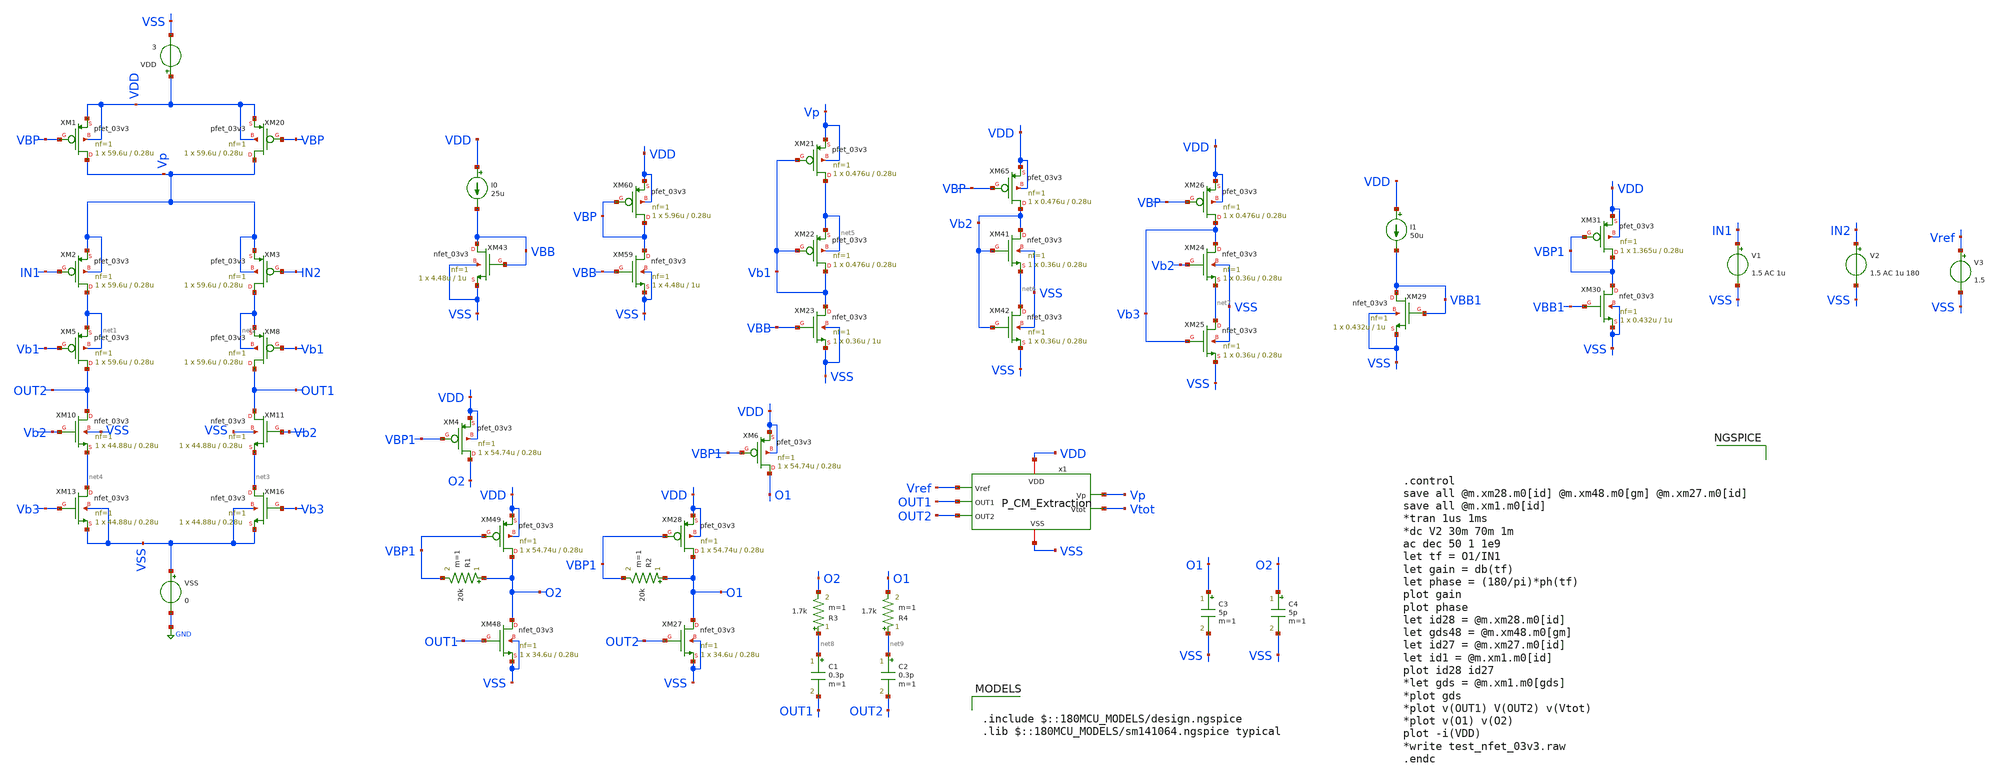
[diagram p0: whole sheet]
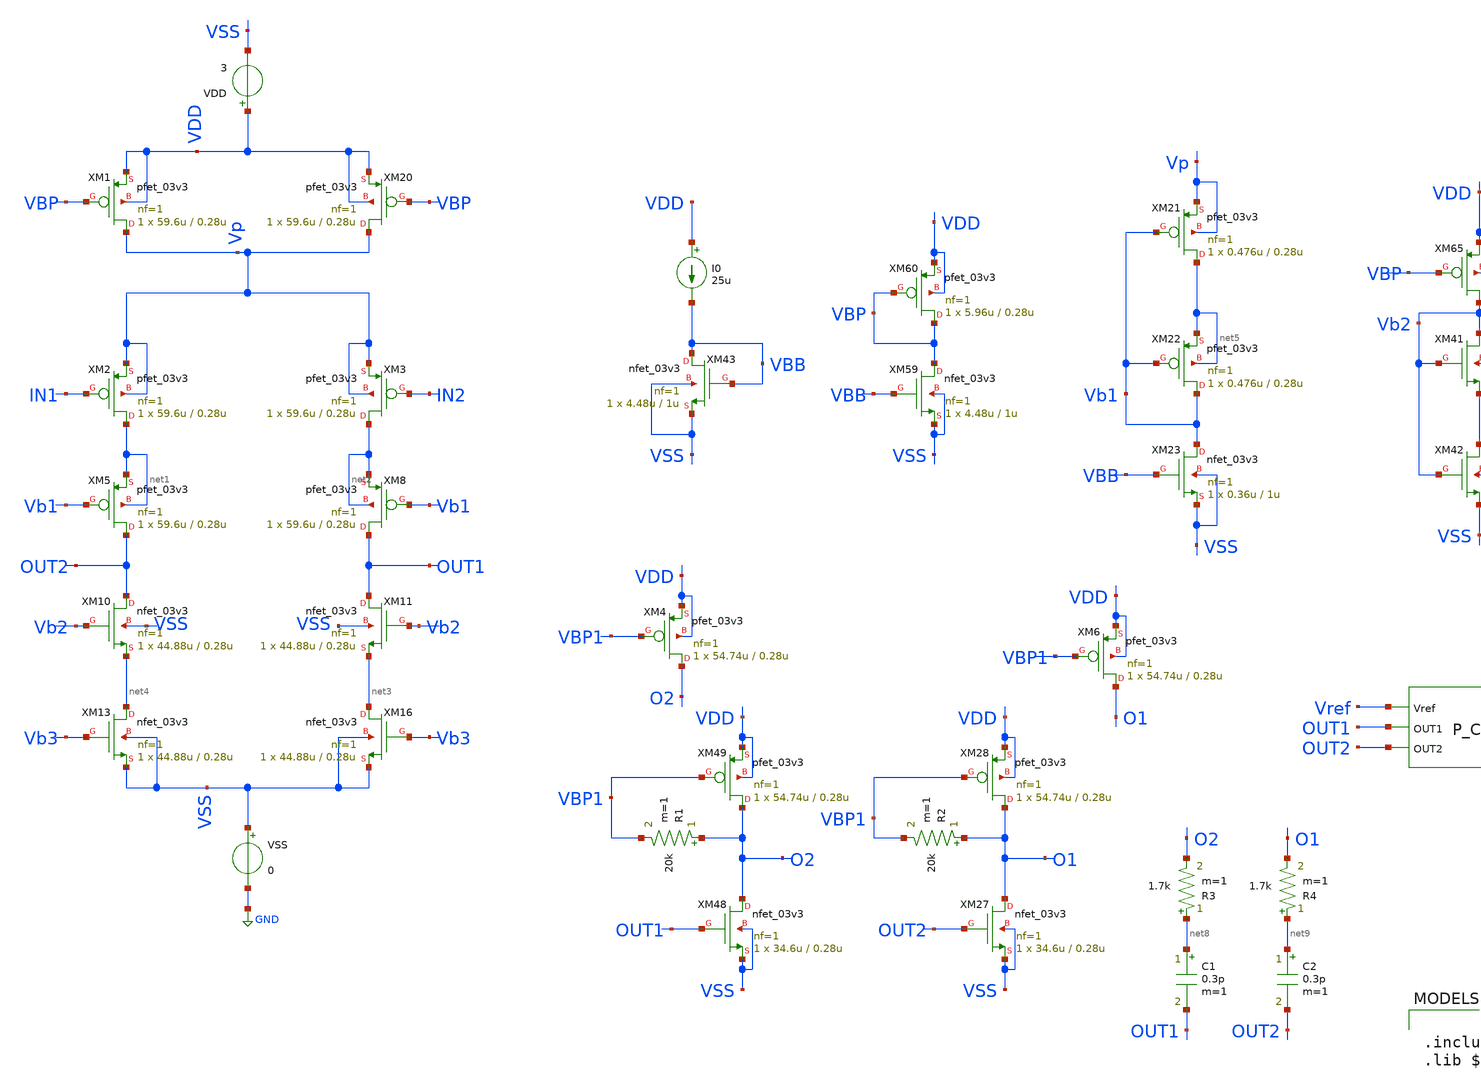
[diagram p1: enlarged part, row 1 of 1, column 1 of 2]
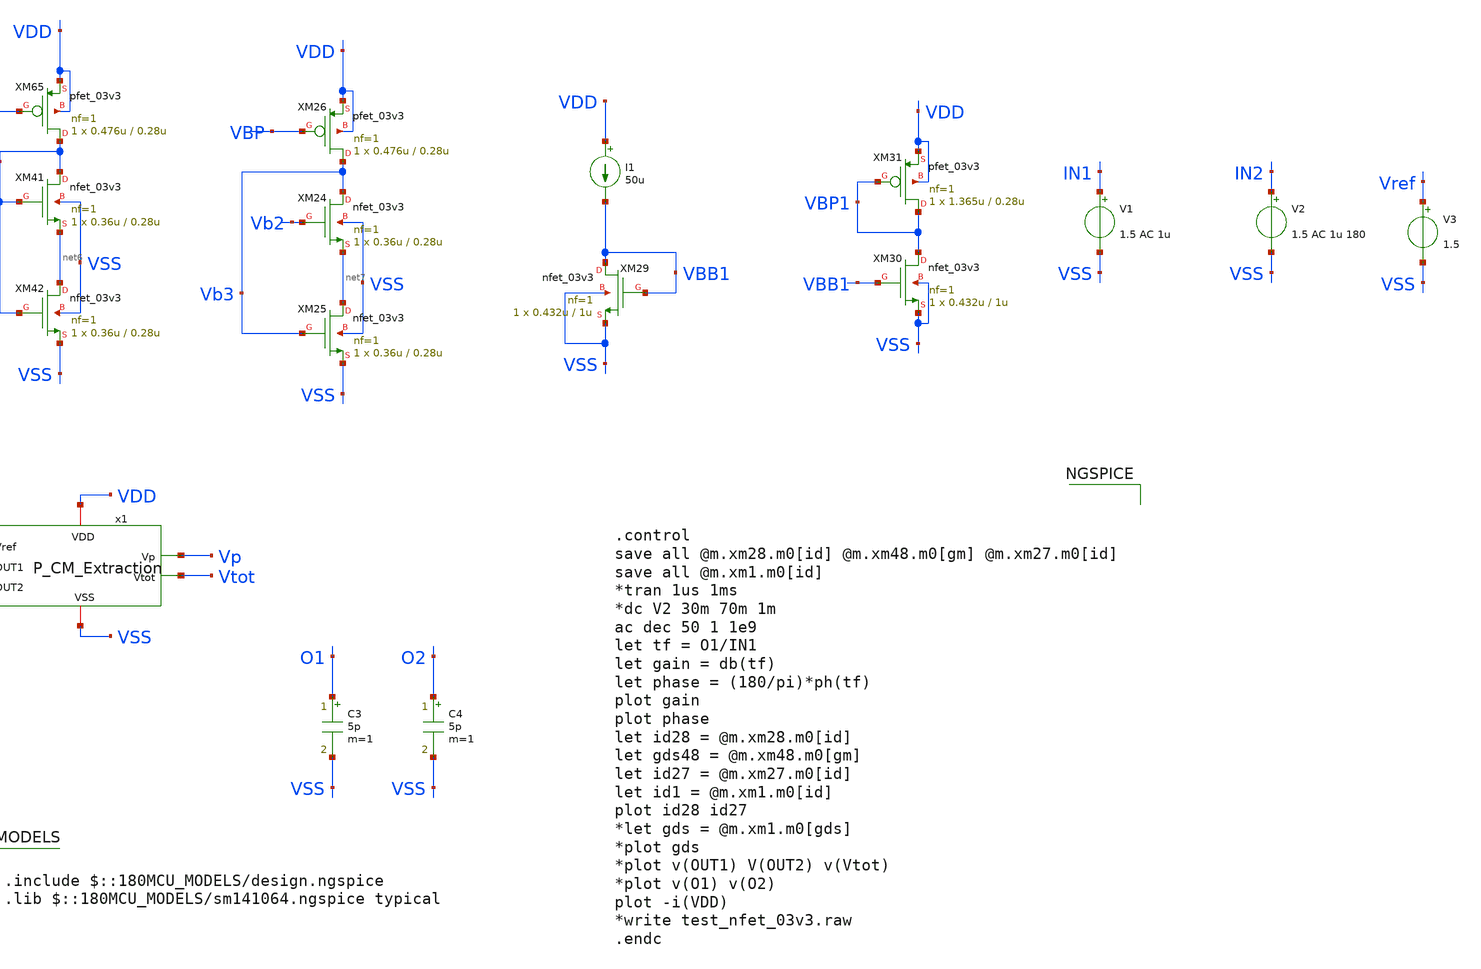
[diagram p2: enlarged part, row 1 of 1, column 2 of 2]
** sch_path: SCOP_INPUT_AND_MUX_PAKISTAN_03/Xschem/Others/PMOS_Diff_Amp.sch
**.subckt PMOS_Diff_Amp
XM2 net1 IN1 Vp Vp pfet_03v3 L=0.28u W=59.6u nf=1 ad='int((nf+1)/2) * W/nf * 0.18u' as='int((nf+2)/2) * W/nf * 0.18u'
+ pd='2*int((nf+1)/2) * (W/nf + 0.18u)' ps='2*int((nf+2)/2) * (W/nf + 0.18u)' nrd='0.18u / W' nrs='0.18u / W'
+ sa=0 sb=0 sd=0 m=1
XM3 net2 IN2 Vp Vp pfet_03v3 L=0.28u W=59.6u nf=1 ad='int((nf+1)/2) * W/nf * 0.18u' as='int((nf+2)/2) * W/nf * 0.18u'
+ pd='2*int((nf+1)/2) * (W/nf + 0.18u)' ps='2*int((nf+2)/2) * (W/nf + 0.18u)' nrd='0.18u / W' nrs='0.18u / W'
+ sa=0 sb=0 sd=0 m=1
XM5 OUT2 Vb1 net1 net1 pfet_03v3 L=0.28u W=59.6u nf=1 ad='int((nf+1)/2) * W/nf * 0.18u' as='int((nf+2)/2) * W/nf * 0.18u'
+ pd='2*int((nf+1)/2) * (W/nf + 0.18u)' ps='2*int((nf+2)/2) * (W/nf + 0.18u)' nrd='0.18u / W' nrs='0.18u / W'
+ sa=0 sb=0 sd=0 m=1
XM8 OUT1 Vb1 net2 net2 pfet_03v3 L=0.28u W=59.6u nf=1 ad='int((nf+1)/2) * W/nf * 0.18u' as='int((nf+2)/2) * W/nf * 0.18u'
+ pd='2*int((nf+1)/2) * (W/nf + 0.18u)' ps='2*int((nf+2)/2) * (W/nf + 0.18u)' nrd='0.18u / W' nrs='0.18u / W'
+ sa=0 sb=0 sd=0 m=1
XM10 OUT2 Vb2 net4 VSS nfet_03v3 L=0.28u W=44.88u nf=1 ad='int((nf+1)/2) * W/nf * 0.18u' as='int((nf+2)/2) * W/nf * 0.18u'
+ pd='2*int((nf+1)/2) * (W/nf + 0.18u)' ps='2*int((nf+2)/2) * (W/nf + 0.18u)' nrd='0.18u / W' nrs='0.18u / W'
+ sa=0 sb=0 sd=0 m=1
XM11 OUT1 Vb2 net3 VSS nfet_03v3 L=0.28u W=44.88u nf=1 ad='int((nf+1)/2) * W/nf * 0.18u' as='int((nf+2)/2) * W/nf * 0.18u'
+ pd='2*int((nf+1)/2) * (W/nf + 0.18u)' ps='2*int((nf+2)/2) * (W/nf + 0.18u)' nrd='0.18u / W' nrs='0.18u / W'
+ sa=0 sb=0 sd=0 m=1
XM13 net4 Vb3 VSS VSS nfet_03v3 L=0.28u W=44.88u nf=1 ad='int((nf+1)/2) * W/nf * 0.18u' as='int((nf+2)/2) * W/nf * 0.18u'
+ pd='2*int((nf+1)/2) * (W/nf + 0.18u)' ps='2*int((nf+2)/2) * (W/nf + 0.18u)' nrd='0.18u / W' nrs='0.18u / W'
+ sa=0 sb=0 sd=0 m=1
XM16 net3 Vb3 VSS VSS nfet_03v3 L=0.28u W=44.88u nf=1 ad='int((nf+1)/2) * W/nf * 0.18u' as='int((nf+2)/2) * W/nf * 0.18u'
+ pd='2*int((nf+1)/2) * (W/nf + 0.18u)' ps='2*int((nf+2)/2) * (W/nf + 0.18u)' nrd='0.18u / W' nrs='0.18u / W'
+ sa=0 sb=0 sd=0 m=1
XM20 Vp VBP VDD VDD pfet_03v3 L=0.28u W=59.6u nf=1 ad='int((nf+1)/2) * W/nf * 0.18u' as='int((nf+2)/2) * W/nf * 0.18u'
+ pd='2*int((nf+1)/2) * (W/nf + 0.18u)' ps='2*int((nf+2)/2) * (W/nf + 0.18u)' nrd='0.18u / W' nrs='0.18u / W'
+ sa=0 sb=0 sd=0 m=1
VSS VSS GND 0
VDD VDD VSS 3
XM1 Vp VBP VDD VDD pfet_03v3 L=0.28u W=59.6u nf=1 ad='int((nf+1)/2) * W/nf * 0.18u' as='int((nf+2)/2) * W/nf * 0.18u'
+ pd='2*int((nf+1)/2) * (W/nf + 0.18u)' ps='2*int((nf+2)/2) * (W/nf + 0.18u)' nrd='0.18u / W' nrs='0.18u / W'
+ sa=0 sb=0 sd=0 m=1
XM43 VBB VBB VSS VSS nfet_03v3 L=1u W=4.48u nf=1 ad='int((nf+1)/2) * W/nf * 0.18u' as='int((nf+2)/2) * W/nf * 0.18u'
+ pd='2*int((nf+1)/2) * (W/nf + 0.18u)' ps='2*int((nf+2)/2) * (W/nf + 0.18u)' nrd='0.18u / W' nrs='0.18u / W'
+ sa=0 sb=0 sd=0 m=1
I0 VDD VBB 25u
XM59 VBP VBB VSS VSS nfet_03v3 L=1u W=4.48u nf=1 ad='int((nf+1)/2) * W/nf * 0.18u' as='int((nf+2)/2) * W/nf * 0.18u'
+ pd='2*int((nf+1)/2) * (W/nf + 0.18u)' ps='2*int((nf+2)/2) * (W/nf + 0.18u)' nrd='0.18u / W' nrs='0.18u / W'
+ sa=0 sb=0 sd=0 m=1
XM60 VBP VBP VDD VDD pfet_03v3 L=0.28u W=5.96u nf=1 ad='int((nf+1)/2) * W/nf * 0.18u' as='int((nf+2)/2) * W/nf * 0.18u'
+ pd='2*int((nf+1)/2) * (W/nf + 0.18u)' ps='2*int((nf+2)/2) * (W/nf + 0.18u)' nrd='0.18u / W' nrs='0.18u / W'
+ sa=0 sb=0 sd=0 m=1
XM21 net5 Vb1 Vp Vp pfet_03v3 L=0.28u W=0.476u nf=1 ad='int((nf+1)/2) * W/nf * 0.18u' as='int((nf+2)/2) * W/nf * 0.18u'
+ pd='2*int((nf+1)/2) * (W/nf + 0.18u)' ps='2*int((nf+2)/2) * (W/nf + 0.18u)' nrd='0.18u / W' nrs='0.18u / W'
+ sa=0 sb=0 sd=0 m=1
XM22 Vb1 Vb1 net5 net5 pfet_03v3 L=0.28u W=0.476u nf=1 ad='int((nf+1)/2) * W/nf * 0.18u' as='int((nf+2)/2) * W/nf * 0.18u'
+ pd='2*int((nf+1)/2) * (W/nf + 0.18u)' ps='2*int((nf+2)/2) * (W/nf + 0.18u)' nrd='0.18u / W' nrs='0.18u / W'
+ sa=0 sb=0 sd=0 m=1
XM23 Vb1 VBB VSS VSS nfet_03v3 L=1u W=0.36u nf=1 ad='int((nf+1)/2) * W/nf * 0.18u' as='int((nf+2)/2) * W/nf * 0.18u'
+ pd='2*int((nf+1)/2) * (W/nf + 0.18u)' ps='2*int((nf+2)/2) * (W/nf + 0.18u)' nrd='0.18u / W' nrs='0.18u / W'
+ sa=0 sb=0 sd=0 m=1
XM41 Vb2 Vb2 net6 VSS nfet_03v3 L=0.28u W=0.36u nf=1 ad='int((nf+1)/2) * W/nf * 0.18u' as='int((nf+2)/2) * W/nf * 0.18u'
+ pd='2*int((nf+1)/2) * (W/nf + 0.18u)' ps='2*int((nf+2)/2) * (W/nf + 0.18u)' nrd='0.18u / W' nrs='0.18u / W'
+ sa=0 sb=0 sd=0 m=1
XM42 net6 Vb2 VSS VSS nfet_03v3 L=0.28u W=0.36u nf=1 ad='int((nf+1)/2) * W/nf * 0.18u' as='int((nf+2)/2) * W/nf * 0.18u'
+ pd='2*int((nf+1)/2) * (W/nf + 0.18u)' ps='2*int((nf+2)/2) * (W/nf + 0.18u)' nrd='0.18u / W' nrs='0.18u / W'
+ sa=0 sb=0 sd=0 m=1
XM65 Vb2 VBP VDD VDD pfet_03v3 L=0.28u W=0.476u nf=1 ad='int((nf+1)/2) * W/nf * 0.18u' as='int((nf+2)/2) * W/nf * 0.18u'
+ pd='2*int((nf+1)/2) * (W/nf + 0.18u)' ps='2*int((nf+2)/2) * (W/nf + 0.18u)' nrd='0.18u / W' nrs='0.18u / W'
+ sa=0 sb=0 sd=0 m=1
XM24 Vb3 Vb2 net7 VSS nfet_03v3 L=0.28u W=0.36u nf=1 ad='int((nf+1)/2) * W/nf * 0.18u' as='int((nf+2)/2) * W/nf * 0.18u'
+ pd='2*int((nf+1)/2) * (W/nf + 0.18u)' ps='2*int((nf+2)/2) * (W/nf + 0.18u)' nrd='0.18u / W' nrs='0.18u / W'
+ sa=0 sb=0 sd=0 m=1
XM25 net7 Vb3 VSS VSS nfet_03v3 L=0.28u W=0.36u nf=1 ad='int((nf+1)/2) * W/nf * 0.18u' as='int((nf+2)/2) * W/nf * 0.18u'
+ pd='2*int((nf+1)/2) * (W/nf + 0.18u)' ps='2*int((nf+2)/2) * (W/nf + 0.18u)' nrd='0.18u / W' nrs='0.18u / W'
+ sa=0 sb=0 sd=0 m=1
XM26 Vb3 VBP VDD VDD pfet_03v3 L=0.28u W=0.476u nf=1 ad='int((nf+1)/2) * W/nf * 0.18u' as='int((nf+2)/2) * W/nf * 0.18u'
+ pd='2*int((nf+1)/2) * (W/nf + 0.18u)' ps='2*int((nf+2)/2) * (W/nf + 0.18u)' nrd='0.18u / W' nrs='0.18u / W'
+ sa=0 sb=0 sd=0 m=1
V1 IN1 VSS 1.5 AC 1u
V2 IN2 VSS 1.5 AC 1u 180
x1 Vref Vp Vtot VDD OUT1 VSS OUT2 P_CM_Extraction
V3 Vref VSS 1.5
XM48 O2 OUT1 VSS VSS nfet_03v3 L=0.28u W=34.6u nf=1 ad='int((nf+1)/2) * W/nf * 0.18u' as='int((nf+2)/2) * W/nf * 0.18u'
+ pd='2*int((nf+1)/2) * (W/nf + 0.18u)' ps='2*int((nf+2)/2) * (W/nf + 0.18u)' nrd='0.18u / W' nrs='0.18u / W'
+ sa=0 sb=0 sd=0 m=1
XM49 O2 VBP1 VDD VDD pfet_03v3 L=0.28u W=54.74u nf=1 ad='int((nf+1)/2) * W/nf * 0.18u' as='int((nf+2)/2) * W/nf * 0.18u'
+ pd='2*int((nf+1)/2) * (W/nf + 0.18u)' ps='2*int((nf+2)/2) * (W/nf + 0.18u)' nrd='0.18u / W' nrs='0.18u / W'
+ sa=0 sb=0 sd=0 m=1
XM27 O1 OUT2 VSS VSS nfet_03v3 L=0.28u W=34.6u nf=1 ad='int((nf+1)/2) * W/nf * 0.18u' as='int((nf+2)/2) * W/nf * 0.18u'
+ pd='2*int((nf+1)/2) * (W/nf + 0.18u)' ps='2*int((nf+2)/2) * (W/nf + 0.18u)' nrd='0.18u / W' nrs='0.18u / W'
+ sa=0 sb=0 sd=0 m=1
XM28 O1 VBP1 VDD VDD pfet_03v3 L=0.28u W=54.74u nf=1 ad='int((nf+1)/2) * W/nf * 0.18u' as='int((nf+2)/2) * W/nf * 0.18u'
+ pd='2*int((nf+1)/2) * (W/nf + 0.18u)' ps='2*int((nf+2)/2) * (W/nf + 0.18u)' nrd='0.18u / W' nrs='0.18u / W'
+ sa=0 sb=0 sd=0 m=1
R1 O2 VBP1 20k m=1
R2 O1 VBP1 20k m=1
XM29 VBB1 VBB1 VSS VSS nfet_03v3 L=1u W=0.432u nf=1 ad='int((nf+1)/2) * W/nf * 0.18u' as='int((nf+2)/2) * W/nf * 0.18u'
+ pd='2*int((nf+1)/2) * (W/nf + 0.18u)' ps='2*int((nf+2)/2) * (W/nf + 0.18u)' nrd='0.18u / W' nrs='0.18u / W'
+ sa=0 sb=0 sd=0 m=1
I1 VDD VBB1 50u
XM30 VBP1 VBB1 VSS VSS nfet_03v3 L=1u W=0.432u nf=1 ad='int((nf+1)/2) * W/nf * 0.18u' as='int((nf+2)/2) * W/nf * 0.18u'
+ pd='2*int((nf+1)/2) * (W/nf + 0.18u)' ps='2*int((nf+2)/2) * (W/nf + 0.18u)' nrd='0.18u / W' nrs='0.18u / W'
+ sa=0 sb=0 sd=0 m=1
XM31 VBP1 VBP1 VDD VDD pfet_03v3 L=0.28u W=1.365u nf=1 ad='int((nf+1)/2) * W/nf * 0.18u' as='int((nf+2)/2) * W/nf * 0.18u'
+ pd='2*int((nf+1)/2) * (W/nf + 0.18u)' ps='2*int((nf+2)/2) * (W/nf + 0.18u)' nrd='0.18u / W' nrs='0.18u / W'
+ sa=0 sb=0 sd=0 m=1
C1 net8 OUT1 0.3p m=1
C2 net9 OUT2 0.3p m=1
R3 net8 O2 1.7k m=1
R4 net9 O1 1.7k m=1
C3 O1 VSS 5p m=1
C4 O2 VSS 5p m=1
XM4 O2 VBP1 VDD VDD pfet_03v3 L=0.28u W=54.74u nf=1 ad='int((nf+1)/2) * W/nf * 0.18u' as='int((nf+2)/2) * W/nf * 0.18u'
+ pd='2*int((nf+1)/2) * (W/nf + 0.18u)' ps='2*int((nf+2)/2) * (W/nf + 0.18u)' nrd='0.18u / W' nrs='0.18u / W'
+ sa=0 sb=0 sd=0 m=1
XM6 O1 VBP1 VDD VDD pfet_03v3 L=0.28u W=54.74u nf=1 ad='int((nf+1)/2) * W/nf * 0.18u' as='int((nf+2)/2) * W/nf * 0.18u'
+ pd='2*int((nf+1)/2) * (W/nf + 0.18u)' ps='2*int((nf+2)/2) * (W/nf + 0.18u)' nrd='0.18u / W' nrs='0.18u / W'
+ sa=0 sb=0 sd=0 m=1
**** begin user architecture code

.include $::180MCU_MODELS/design.ngspice
.lib $::180MCU_MODELS/sm141064.ngspice typical




.control
save all @m.xm28.m0[id] @m.xm48.m0[gm] @m.xm27.m0[id]
save all @m.xm1.m0[id]
*tran 1us 1ms
*dc V2 30m 70m 1m
ac dec 50 1 1e9
let tf = O1/IN1
let gain = db(tf)
let phase = (180/pi)*ph(tf)
plot gain
plot phase
let id28 = @m.xm28.m0[id]
let gds48 = @m.xm48.m0[gm]
let id27 = @m.xm27.m0[id]
let id1 = @m.xm1.m0[id]
plot id28 id27
*let gds = @m.xm1.m0[gds]
*plot gds
*plot v(OUT1) V(OUT2) v(Vtot)
*plot v(O1) v(O2)
plot -i(VDD)
*write test_nfet_03v3.raw
.endc


**** end user architecture code
**.ends

* expanding   symbol:  Tapeout/P_CM_Extraction.sym # of pins=7
** sym_path: SCOP_INPUT_AND_MUX_PAKISTAN_03/Xschem/Others/P_CM_Extraction.sym
** sch_path: SCOP_INPUT_AND_MUX_PAKISTAN_03/Xschem/Others/P_CM_Extraction.sch
.subckt P_CM_Extraction Vref Vp Vtot VDD OUT1 VSS OUT2
*.ipin Vref
*.ipin OUT1
*.ipin OUT2
*.opin Vp
*.iopin VDD
*.iopin VSS
*.opin Vtot
R2 Vtot OUT1 50k m=1
R4 OUT2 Vtot 50k m=1
XM59 VBP VBB VSS VSS nfet_03v3 L=1u W=4.48u nf=1 ad='int((nf+1)/2) * W/nf * 0.18u' as='int((nf+2)/2) * W/nf * 0.18u'
+ pd='2*int((nf+1)/2) * (W/nf + 0.18u)' ps='2*int((nf+2)/2) * (W/nf + 0.18u)' nrd='0.18u / W' nrs='0.18u / W'
+ sa=0 sb=0 sd=0 m=1
XM60 VBP VBP VDD VDD pfet_03v3 L=0.28u W=5.96u nf=1 ad='int((nf+1)/2) * W/nf * 0.18u' as='int((nf+2)/2) * W/nf * 0.18u'
+ pd='2*int((nf+1)/2) * (W/nf + 0.18u)' ps='2*int((nf+2)/2) * (W/nf + 0.18u)' nrd='0.18u / W' nrs='0.18u / W'
+ sa=0 sb=0 sd=0 m=1
XM43 VBB VBB VSS VSS nfet_03v3 L=1u W=4.48u nf=1 ad='int((nf+1)/2) * W/nf * 0.18u' as='int((nf+2)/2) * W/nf * 0.18u'
+ pd='2*int((nf+1)/2) * (W/nf + 0.18u)' ps='2*int((nf+2)/2) * (W/nf + 0.18u)' nrd='0.18u / W' nrs='0.18u / W'
+ sa=0 sb=0 sd=0 m=1
I0 VDD VBB 25u
XM1 net1 net1 VDD VDD pfet_03v3 L=0.28u W=5.96u nf=1 ad='int((nf+1)/2) * W/nf * 0.18u' as='int((nf+2)/2) * W/nf * 0.18u'
+ pd='2*int((nf+1)/2) * (W/nf + 0.18u)' ps='2*int((nf+2)/2) * (W/nf + 0.18u)' nrd='0.18u / W' nrs='0.18u / W'
+ sa=0 sb=0 sd=0 m=1
XM2 Vp net1 VDD VDD pfet_03v3 L=0.28u W=5.96u nf=1 ad='int((nf+1)/2) * W/nf * 0.18u' as='int((nf+2)/2) * W/nf * 0.18u'
+ pd='2*int((nf+1)/2) * (W/nf + 0.18u)' ps='2*int((nf+2)/2) * (W/nf + 0.18u)' nrd='0.18u / W' nrs='0.18u / W'
+ sa=0 sb=0 sd=0 m=1
XM3 net1 Vtot net2 VSS nfet_03v3 L=0.28u W=4.48u nf=1 ad='int((nf+1)/2) * W/nf * 0.18u' as='int((nf+2)/2) * W/nf * 0.18u'
+ pd='2*int((nf+1)/2) * (W/nf + 0.18u)' ps='2*int((nf+2)/2) * (W/nf + 0.18u)' nrd='0.18u / W' nrs='0.18u / W'
+ sa=0 sb=0 sd=0 m=1
XM4 Vp Vref net2 VSS nfet_03v3 L=0.28u W=4.48u nf=1 ad='int((nf+1)/2) * W/nf * 0.18u' as='int((nf+2)/2) * W/nf * 0.18u'
+ pd='2*int((nf+1)/2) * (W/nf + 0.18u)' ps='2*int((nf+2)/2) * (W/nf + 0.18u)' nrd='0.18u / W' nrs='0.18u / W'
+ sa=0 sb=0 sd=0 m=1
XM5 net2 VBB VSS VSS nfet_03v3 L=1u W=4.48u nf=1 ad='int((nf+1)/2) * W/nf * 0.18u' as='int((nf+2)/2) * W/nf * 0.18u'
+ pd='2*int((nf+1)/2) * (W/nf + 0.18u)' ps='2*int((nf+2)/2) * (W/nf + 0.18u)' nrd='0.18u / W' nrs='0.18u / W'
+ sa=0 sb=0 sd=0 m=1
.ends

.GLOBAL GND
.end
